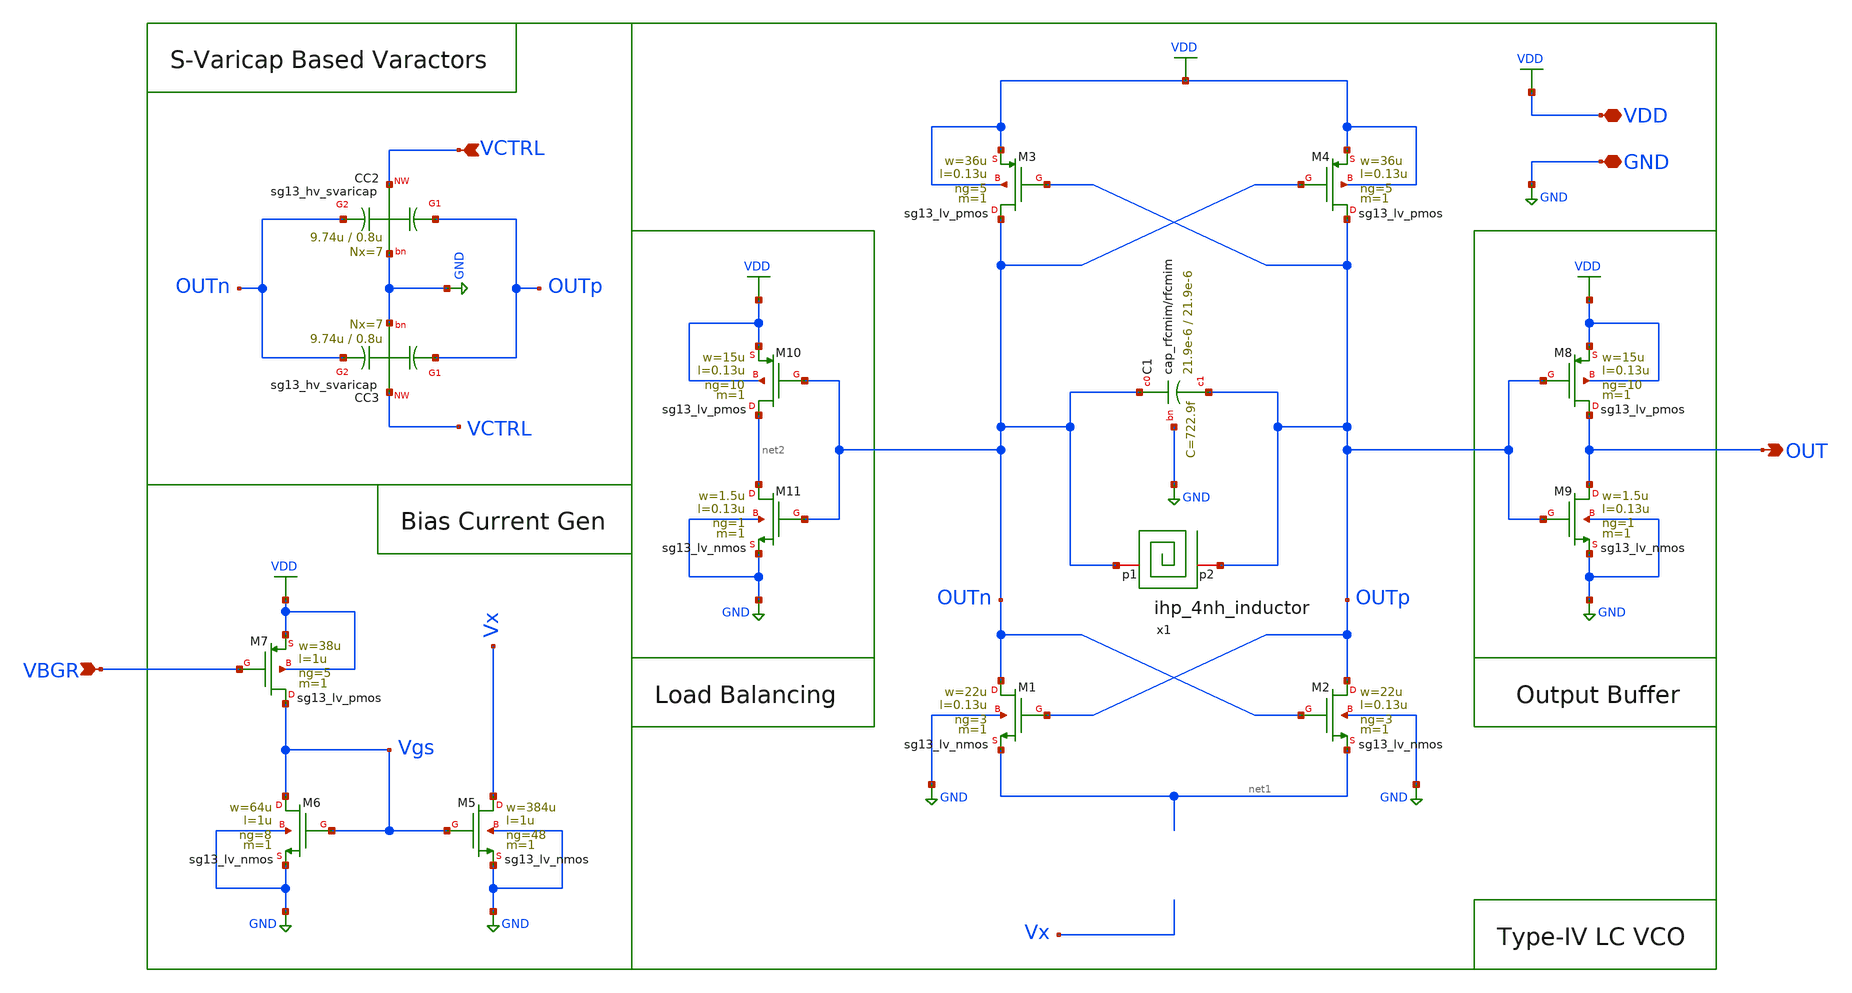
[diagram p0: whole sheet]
** sch_path: schematic/lc-vco/LC_VCO.sch
**.subckt LC_VCO OUT VCTRL VBGR VDD GND
*.opin OUT
*.ipin VCTRL
*.ipin VBGR
*.iopin VDD
*.iopin GND
XM5 Vx Vgs GND GND sg13_lv_nmos w=384u l=1u ng=48 m=1 mm_ok=1
XM4 OUTp OUTn VDD VDD sg13_lv_pmos w=36u l=0.13u ng=5 m=1 mm_ok=1
XM3 OUTn OUTp VDD VDD sg13_lv_pmos w=36u l=0.13u ng=5 m=1 mm_ok=1
XM2 OUTp OUTn net1 GND sg13_lv_nmos w=22u l=0.13u ng=3 m=1 mm_ok=1
XM1 OUTn OUTp net1 GND sg13_lv_nmos w=22u l=0.13u ng=3 m=1 mm_ok=1
XM6 Vgs Vgs GND GND sg13_lv_nmos w=64u l=1u ng=8 m=1 mm_ok=1
x1 OUTn OUTp ihp_4nh_inductor
XC1 OUTn OUTp GND cap_rfcmim w=21.9e-6 l=21.9e-6 wfeed=10.0e-6 m=1 mm_ok=1
XC3 OUTp VCTRL OUTn GND sg13_hv_svaricap w=9.74u l=0.8u Nx=7
XC2 OUTp VCTRL OUTn GND sg13_hv_svaricap w=9.74u l=0.8u Nx=7
XM7 Vgs VBGR VDD VDD sg13_lv_pmos w=38u l=1u ng=5 m=1 mm_ok=1
XM8 OUT OUTp VDD VDD sg13_lv_pmos w=15u l=0.13u ng=10 m=1 mm_ok=1
XM9 OUT OUTp GND GND sg13_lv_nmos w=1.5u l=0.13u ng=1 m=1 mm_ok=1
XM10 net2 OUTn VDD VDD sg13_lv_pmos w=15u l=0.13u ng=10 m=1 mm_ok=1
XM11 net2 OUTn GND GND sg13_lv_nmos w=1.5u l=0.13u ng=1 m=1 mm_ok=1
**.ends
.GLOBAL GND
.GLOBAL VDD
.end
